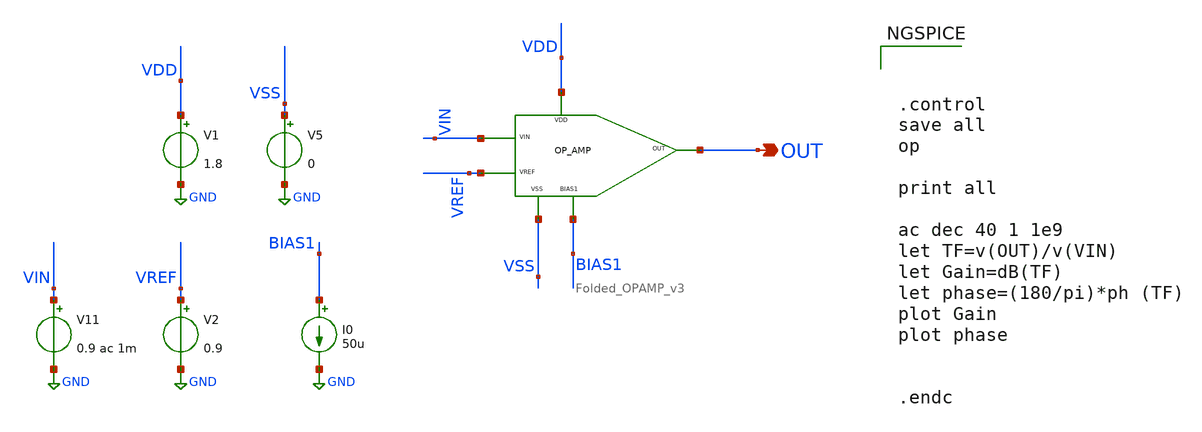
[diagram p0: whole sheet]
** sch_path: xschem/DC_DC_Converter_xschem/OTHERS/DC_DC_Converter_4/Folded_OPAMP/TB_Folded_OPAMP_v3.sch
**.subckt TB_Folded_OPAMP_v3 OUT
*.opin OUT
I0 BIAS1 GND 50u
V1 VDD GND 1.8
V5 VSS GND 0
V11 VIN GND 0.9 ac 1m
V2 VREF GND 0.9
x1 VDD VSS BIAS1 OUT VIN VREF Folded_OPAMP_v3
**** begin user architecture code

** opencircuitdesign pdks install
.lib $::SKYWATER_MODELS/sky130.lib.spice tt





.control
save all
op

print all

ac dec 40 1 1e9
let TF=v(OUT)/v(VIN)
let Gain=dB(TF)
let phase=(180/pi)*ph (TF)
plot Gain
plot phase


.endc


**** end user architecture code
**.ends
.GLOBAL GND
.end
